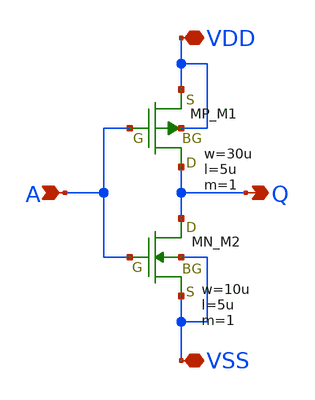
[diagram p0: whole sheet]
** sch_path: member_project/AM_Radio/Yamada3/xschem/inverter.sch
**.subckt inverter VDD VSS A Q
*.iopin VDD
*.iopin VSS
*.ipin A
*.opin Q
XM1 Q A VDD VDD PMOS w=30u l=5u as=0 ad=0 ps=0 pd=0 nrd=0 nrs=0 m=1
XM2 Q A VSS VSS NMOS w=10u l=5u as=0 ad=0 ps=0 pd=0 nrd=0 nrs=0 m=1
**.ends
.end
